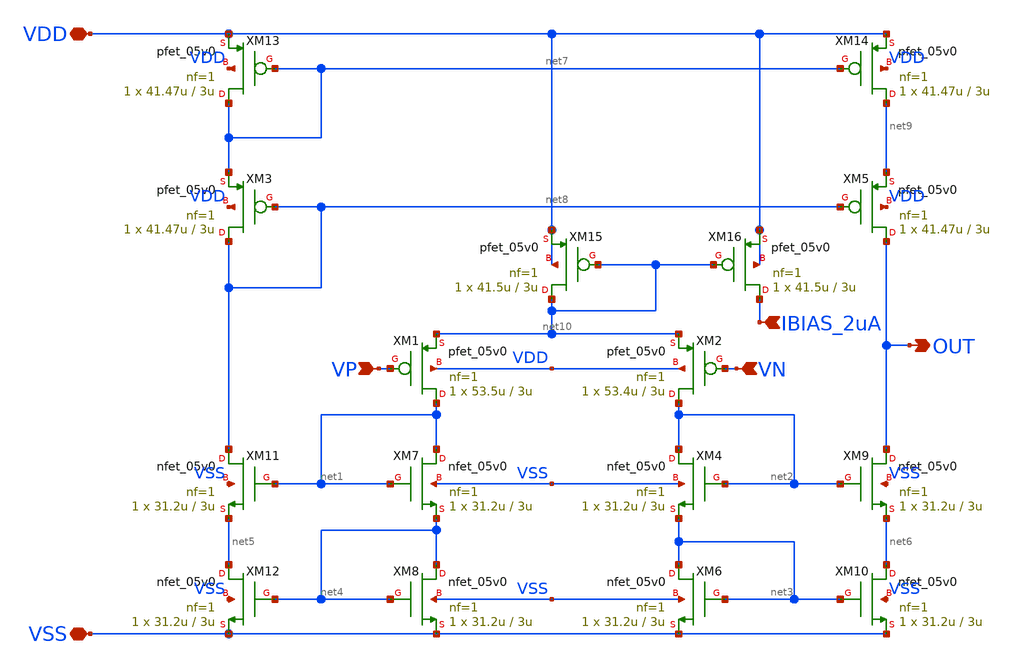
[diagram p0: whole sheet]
** sch_path: designs/symmetrical-ota-2/symmetrical-ota-2.sch
**.subckt symmetrical-ota-2 VDD VSS OUT IBIAS_2uA VP VN
*.iopin VDD
*.iopin VSS
*.opin OUT
*.ipin IBIAS_2uA
*.ipin VP
*.ipin VN
XM1 net1 VP net10 VDD pfet_05v0 L=3u W=53.5u nf=1 ad='int((nf+1)/2) * W/nf * 0.18u' as='int((nf+2)/2) * W/nf * 0.18u'
+ pd='2*int((nf+1)/2) * (W/nf + 0.18u)' ps='2*int((nf+2)/2) * (W/nf + 0.18u)' nrd='0.18u / W' nrs='0.18u / W'
+ sa=0 sb=0 sd=0 m=1
XM2 net2 VN net10 VDD pfet_05v0 L=3u W=53.4u nf=1 ad='int((nf+1)/2) * W/nf * 0.18u' as='int((nf+2)/2) * W/nf * 0.18u'
+ pd='2*int((nf+1)/2) * (W/nf + 0.18u)' ps='2*int((nf+2)/2) * (W/nf + 0.18u)' nrd='0.18u / W' nrs='0.18u / W'
+ sa=0 sb=0 sd=0 m=1
XM4 net2 net2 net3 VSS nfet_05v0 L=3u W=31.2u nf=1 ad='int((nf+1)/2) * W/nf * 0.18u' as='int((nf+2)/2) * W/nf * 0.18u'
+ pd='2*int((nf+1)/2) * (W/nf + 0.18u)' ps='2*int((nf+2)/2) * (W/nf + 0.18u)' nrd='0.18u / W' nrs='0.18u / W'
+ sa=0 sb=0 sd=0 m=1
XM6 net3 net3 VSS VSS nfet_05v0 L=3u W=31.2u nf=1 ad='int((nf+1)/2) * W/nf * 0.18u' as='int((nf+2)/2) * W/nf * 0.18u'
+ pd='2*int((nf+1)/2) * (W/nf + 0.18u)' ps='2*int((nf+2)/2) * (W/nf + 0.18u)' nrd='0.18u / W' nrs='0.18u / W'
+ sa=0 sb=0 sd=0 m=1
XM7 net1 net1 net4 VSS nfet_05v0 L=3u W=31.2u nf=1 ad='int((nf+1)/2) * W/nf * 0.18u' as='int((nf+2)/2) * W/nf * 0.18u'
+ pd='2*int((nf+1)/2) * (W/nf + 0.18u)' ps='2*int((nf+2)/2) * (W/nf + 0.18u)' nrd='0.18u / W' nrs='0.18u / W'
+ sa=0 sb=0 sd=0 m=1
XM8 net4 net4 VSS VSS nfet_05v0 L=3u W=31.2u nf=1 ad='int((nf+1)/2) * W/nf * 0.18u' as='int((nf+2)/2) * W/nf * 0.18u'
+ pd='2*int((nf+1)/2) * (W/nf + 0.18u)' ps='2*int((nf+2)/2) * (W/nf + 0.18u)' nrd='0.18u / W' nrs='0.18u / W'
+ sa=0 sb=0 sd=0 m=1
XM9 OUT net2 net6 VSS nfet_05v0 L=3u W=31.2u nf=1 ad='int((nf+1)/2) * W/nf * 0.18u' as='int((nf+2)/2) * W/nf * 0.18u'
+ pd='2*int((nf+1)/2) * (W/nf + 0.18u)' ps='2*int((nf+2)/2) * (W/nf + 0.18u)' nrd='0.18u / W' nrs='0.18u / W'
+ sa=0 sb=0 sd=0 m=1
XM10 net6 net3 VSS VSS nfet_05v0 L=3u W=31.2u nf=1 ad='int((nf+1)/2) * W/nf * 0.18u' as='int((nf+2)/2) * W/nf * 0.18u'
+ pd='2*int((nf+1)/2) * (W/nf + 0.18u)' ps='2*int((nf+2)/2) * (W/nf + 0.18u)' nrd='0.18u / W' nrs='0.18u / W'
+ sa=0 sb=0 sd=0 m=1
XM11 net8 net1 net5 VSS nfet_05v0 L=3u W=31.2u nf=1 ad='int((nf+1)/2) * W/nf * 0.18u' as='int((nf+2)/2) * W/nf * 0.18u'
+ pd='2*int((nf+1)/2) * (W/nf + 0.18u)' ps='2*int((nf+2)/2) * (W/nf + 0.18u)' nrd='0.18u / W' nrs='0.18u / W'
+ sa=0 sb=0 sd=0 m=1
XM12 net5 net4 VSS VSS nfet_05v0 L=3u W=31.2u nf=1 ad='int((nf+1)/2) * W/nf * 0.18u' as='int((nf+2)/2) * W/nf * 0.18u'
+ pd='2*int((nf+1)/2) * (W/nf + 0.18u)' ps='2*int((nf+2)/2) * (W/nf + 0.18u)' nrd='0.18u / W' nrs='0.18u / W'
+ sa=0 sb=0 sd=0 m=1
XM3 net8 net8 net7 VDD pfet_05v0 L=3u W=41.47u nf=1 ad='int((nf+1)/2) * W/nf * 0.18u' as='int((nf+2)/2) * W/nf * 0.18u'
+ pd='2*int((nf+1)/2) * (W/nf + 0.18u)' ps='2*int((nf+2)/2) * (W/nf + 0.18u)' nrd='0.18u / W' nrs='0.18u / W'
+ sa=0 sb=0 sd=0 m=1
XM5 OUT net8 net9 VDD pfet_05v0 L=3u W=41.47u nf=1 ad='int((nf+1)/2) * W/nf * 0.18u' as='int((nf+2)/2) * W/nf * 0.18u'
+ pd='2*int((nf+1)/2) * (W/nf + 0.18u)' ps='2*int((nf+2)/2) * (W/nf + 0.18u)' nrd='0.18u / W' nrs='0.18u / W'
+ sa=0 sb=0 sd=0 m=1
XM13 net7 net7 VDD VDD pfet_05v0 L=3u W=41.47u nf=1 ad='int((nf+1)/2) * W/nf * 0.18u' as='int((nf+2)/2) * W/nf * 0.18u'
+ pd='2*int((nf+1)/2) * (W/nf + 0.18u)' ps='2*int((nf+2)/2) * (W/nf + 0.18u)' nrd='0.18u / W' nrs='0.18u / W'
+ sa=0 sb=0 sd=0 m=1
XM14 net9 net7 VDD VDD pfet_05v0 L=3u W=41.47u nf=1 ad='int((nf+1)/2) * W/nf * 0.18u' as='int((nf+2)/2) * W/nf * 0.18u'
+ pd='2*int((nf+1)/2) * (W/nf + 0.18u)' ps='2*int((nf+2)/2) * (W/nf + 0.18u)' nrd='0.18u / W' nrs='0.18u / W'
+ sa=0 sb=0 sd=0 m=1
XM15 net10 net10 VDD VDD pfet_05v0 L=3u W=41.5u nf=1 ad='int((nf+1)/2) * W/nf * 0.18u' as='int((nf+2)/2) * W/nf * 0.18u'
+ pd='2*int((nf+1)/2) * (W/nf + 0.18u)' ps='2*int((nf+2)/2) * (W/nf + 0.18u)' nrd='0.18u / W' nrs='0.18u / W'
+ sa=0 sb=0 sd=0 m=1
XM16 IBIAS_2uA net10 VDD VDD pfet_05v0 L=3u W=41.5u nf=1 ad='int((nf+1)/2) * W/nf * 0.18u' as='int((nf+2)/2) * W/nf * 0.18u'
+ pd='2*int((nf+1)/2) * (W/nf + 0.18u)' ps='2*int((nf+2)/2) * (W/nf + 0.18u)' nrd='0.18u / W' nrs='0.18u / W'
+ sa=0 sb=0 sd=0 m=1
**.ends
.end
